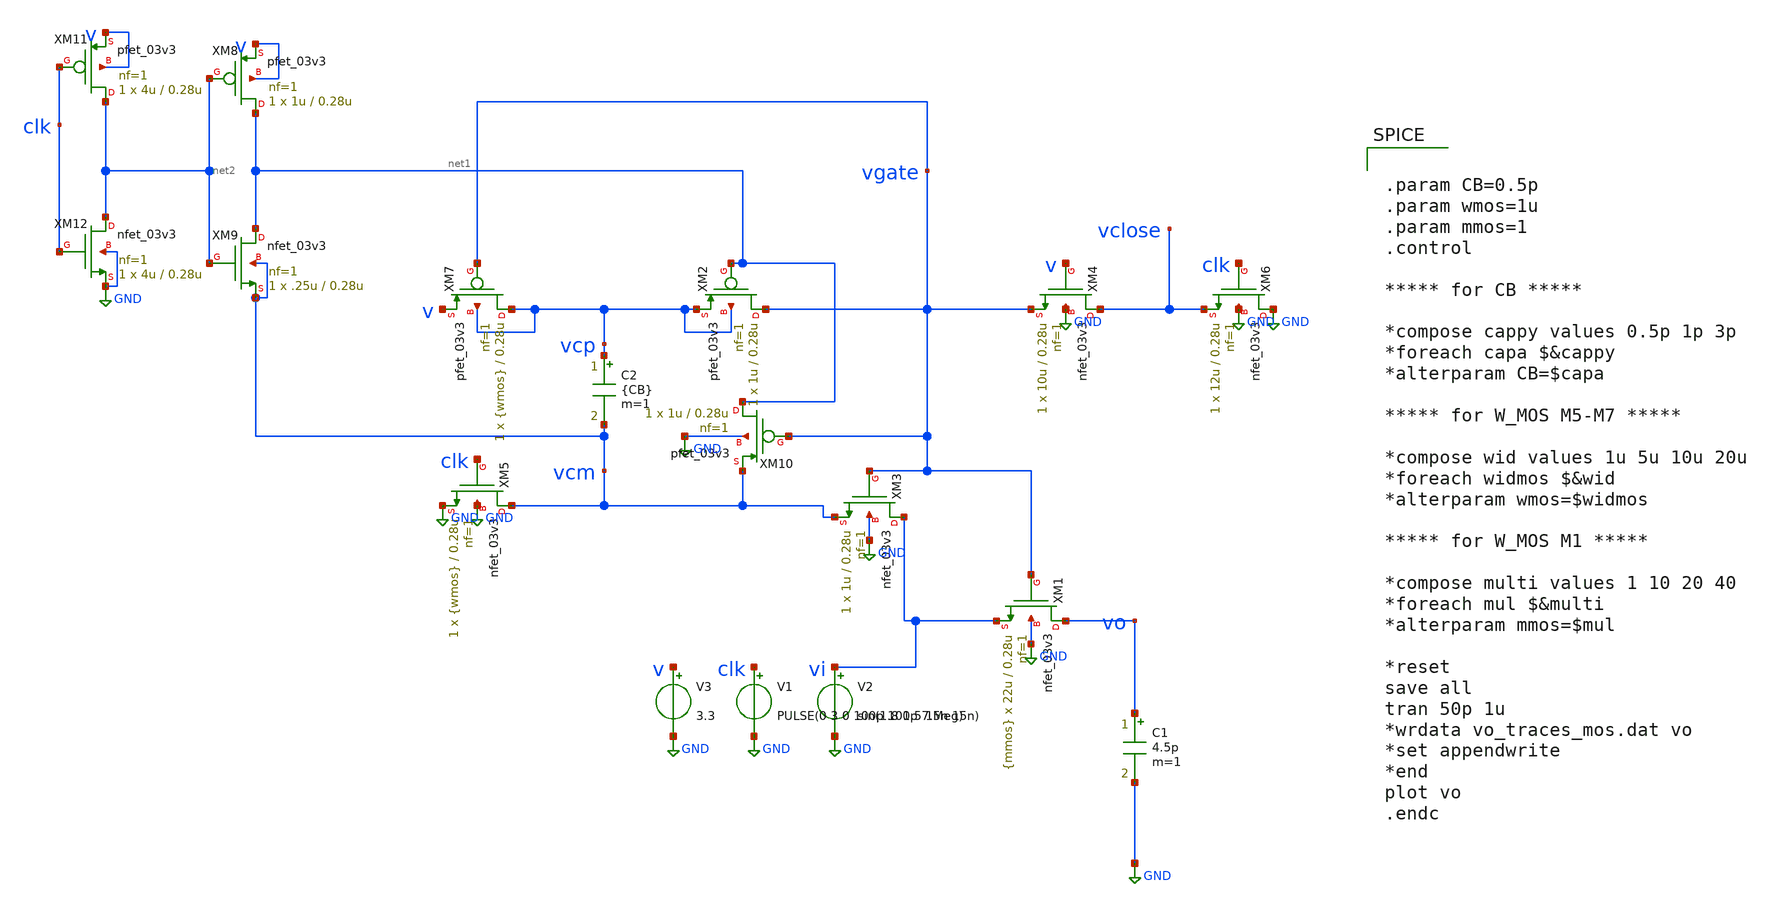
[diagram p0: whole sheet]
** sch_path: bootstrap_switch/bootstrap_sw_design.sch
**.subckt bootstrap_sw_design
XM1 vo vgate vi GND nfet_03v3 L=0.28u W=22u nf=1 ad='int((nf+1)/2) * W/nf * 0.18u' as='int((nf+2)/2) * W/nf * 0.18u'
+ pd='2*int((nf+1)/2) * (W/nf + 0.18u)' ps='2*int((nf+2)/2) * (W/nf + 0.18u)' nrd='0.18u / W' nrs='0.18u / W'
+ sa=0 sb=0 sd=0 m={mmos}
XM2 vgate net1 vcp vcp pfet_03v3 L=0.28u W=1u nf=1 ad='int((nf+1)/2) * W/nf * 0.18u' as='int((nf+2)/2) * W/nf * 0.18u'
+ pd='2*int((nf+1)/2) * (W/nf + 0.18u)' ps='2*int((nf+2)/2) * (W/nf + 0.18u)' nrd='0.18u / W' nrs='0.18u / W'
+ sa=0 sb=0 sd=0 m=1
XM3 vi vgate vcm GND nfet_03v3 L=0.28u W=1u nf=1 ad='int((nf+1)/2) * W/nf * 0.18u' as='int((nf+2)/2) * W/nf * 0.18u'
+ pd='2*int((nf+1)/2) * (W/nf + 0.18u)' ps='2*int((nf+2)/2) * (W/nf + 0.18u)' nrd='0.18u / W' nrs='0.18u / W'
+ sa=0 sb=0 sd=0 m=1
XM4 vclose v vgate GND nfet_03v3 L=0.28u W=10u nf=1 ad='int((nf+1)/2) * W/nf * 0.18u' as='int((nf+2)/2) * W/nf * 0.18u'
+ pd='2*int((nf+1)/2) * (W/nf + 0.18u)' ps='2*int((nf+2)/2) * (W/nf + 0.18u)' nrd='0.18u / W' nrs='0.18u / W'
+ sa=0 sb=0 sd=0 m=1
XM5 vcm clk GND GND nfet_03v3 L=0.28u W={wmos} nf=1 ad='int((nf+1)/2) * W/nf * 0.18u' as='int((nf+2)/2) * W/nf * 0.18u'
+ pd='2*int((nf+1)/2) * (W/nf + 0.18u)' ps='2*int((nf+2)/2) * (W/nf + 0.18u)' nrd='0.18u / W' nrs='0.18u / W'
+ sa=0 sb=0 sd=0 m=1
XM6 GND clk vclose GND nfet_03v3 L=0.28u W=12u nf=1 ad='int((nf+1)/2) * W/nf * 0.18u' as='int((nf+2)/2) * W/nf * 0.18u'
+ pd='2*int((nf+1)/2) * (W/nf + 0.18u)' ps='2*int((nf+2)/2) * (W/nf + 0.18u)' nrd='0.18u / W' nrs='0.18u / W'
+ sa=0 sb=0 sd=0 m=1
XM7 vcp vgate v vcp pfet_03v3 L=0.28u W={wmos} nf=1 ad='int((nf+1)/2) * W/nf * 0.18u' as='int((nf+2)/2) * W/nf * 0.18u'
+ pd='2*int((nf+1)/2) * (W/nf + 0.18u)' ps='2*int((nf+2)/2) * (W/nf + 0.18u)' nrd='0.18u / W' nrs='0.18u / W'
+ sa=0 sb=0 sd=0 m=1
V1 clk GND PULSE(0 3 0 100p 100p 7.5n 15n)
V2 vi GND sin(1.8 1.5 1Meg)
V3 v GND 3.3
XM8 net1 net2 v v pfet_03v3 L=0.28u W=1u nf=1 ad='int((nf+1)/2) * W/nf * 0.18u' as='int((nf+2)/2) * W/nf * 0.18u'
+ pd='2*int((nf+1)/2) * (W/nf + 0.18u)' ps='2*int((nf+2)/2) * (W/nf + 0.18u)' nrd='0.18u / W' nrs='0.18u / W'
+ sa=0 sb=0 sd=0 m=1
XM9 net1 net2 vcm vcm nfet_03v3 L=0.28u W=.25u nf=1 ad='int((nf+1)/2) * W/nf * 0.18u' as='int((nf+2)/2) * W/nf * 0.18u'
+ pd='2*int((nf+1)/2) * (W/nf + 0.18u)' ps='2*int((nf+2)/2) * (W/nf + 0.18u)' nrd='0.18u / W' nrs='0.18u / W'
+ sa=0 sb=0 sd=0 m=1
XM10 net1 vgate vcm GND pfet_03v3 L=0.28u W=1u nf=1 ad='int((nf+1)/2) * W/nf * 0.18u' as='int((nf+2)/2) * W/nf * 0.18u'
+ pd='2*int((nf+1)/2) * (W/nf + 0.18u)' ps='2*int((nf+2)/2) * (W/nf + 0.18u)' nrd='0.18u / W' nrs='0.18u / W'
+ sa=0 sb=0 sd=0 m=1
XM11 net2 clk v v pfet_03v3 L=0.28u W=4u nf=1 ad='int((nf+1)/2) * W/nf * 0.18u' as='int((nf+2)/2) * W/nf * 0.18u'
+ pd='2*int((nf+1)/2) * (W/nf + 0.18u)' ps='2*int((nf+2)/2) * (W/nf + 0.18u)' nrd='0.18u / W' nrs='0.18u / W'
+ sa=0 sb=0 sd=0 m=1
XM12 net2 clk GND GND nfet_03v3 L=0.28u W=4u nf=1 ad='int((nf+1)/2) * W/nf * 0.18u' as='int((nf+2)/2) * W/nf * 0.18u'
+ pd='2*int((nf+1)/2) * (W/nf + 0.18u)' ps='2*int((nf+2)/2) * (W/nf + 0.18u)' nrd='0.18u / W' nrs='0.18u / W'
+ sa=0 sb=0 sd=0 m=1
C1 vo GND 4.5p m=1
C2 vcp vcm {CB} m=1
**** begin user architecture code


.param CB=0.5p
.param wmos=1u
.param mmos=1
.control

***** for CB *****

*compose cappy values 0.5p 1p 3p
*foreach capa $&cappy
*alterparam CB=$capa

***** for W_MOS M5-M7 *****

*compose wid values 1u 5u 10u 20u
*foreach widmos $&wid
*alterparam wmos=$widmos

***** for W_MOS M1 *****

*compose multi values 1 10 20 40
*foreach mul $&multi
*alterparam mmos=$mul

*reset
save all
tran 50p 1u
*wrdata vo_traces_mos.dat vo
*set appendwrite
*end
plot vo
.endc


.include /foss/pdks/gf180mcuC/libs.tech/ngspice/design.ngspice
.lib /foss/pdks/gf180mcuC/libs.tech/ngspice/sm141064.ngspice typical
.lib /foss/pdks/gf180mcuC/libs.tech/ngspice/sm141064.ngspice mimcap_statistical
.lib /foss/pdks/gf180mcuC/libs.tech/ngspice/sm141064.ngspice cap_mim

**** end user architecture code
**.ends
.GLOBAL GND
.end
